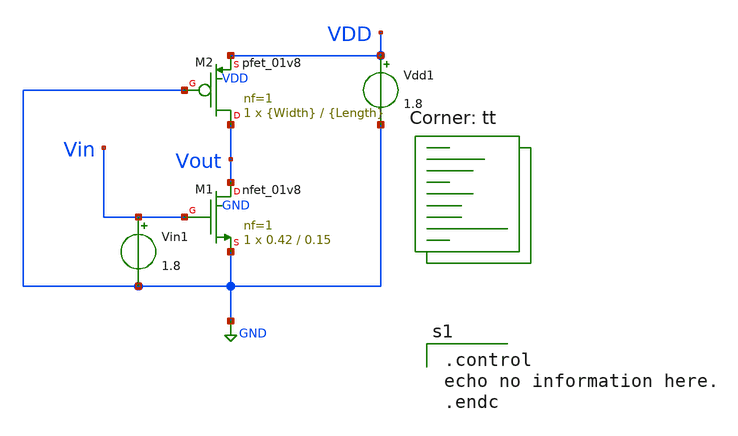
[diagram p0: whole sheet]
** sch_path: tut2/expt1/expt1.sch
**.subckt expt1
XM1 Vout Vin GND GND sky130_fd_pr__nfet_01v8 L=0.15 W=0.42 nf=1 ad='int((nf+1)/2) * W/nf * 0.29' as='int((nf+2)/2) * W/nf * 0.29'
+ pd='2*int((nf+1)/2) * (W/nf + 0.29)' ps='2*int((nf+2)/2) * (W/nf + 0.29)' nrd='0.29 / W' nrs='0.29 / W'
+ sa=0 sb=0 sd=0 mult=1 m=1
Vin1 Vin GND 1.8
XM2 Vout GND VDD VDD sky130_fd_pr__pfet_01v8 L={Length} W={Width} nf=1 ad='int((nf+1)/2) * W/nf * 0.29'
+ as='int((nf+2)/2) * W/nf * 0.29' pd='2*int((nf+1)/2) * (W/nf + 0.29)' ps='2*int((nf+2)/2) * (W/nf + 0.29)'
+ nrd='0.29 / W' nrs='0.29 / W' sa=0 sb=0 sd=0 mult=1 m=1
Vdd1 VDD GND 1.8
**** begin user architecture code
.lib $::SKYWATER_MODELS/sky130.lib.spice tt

.control
echo no information here.
.endc

**** end user architecture code
**.ends
.GLOBAL GND
.end
